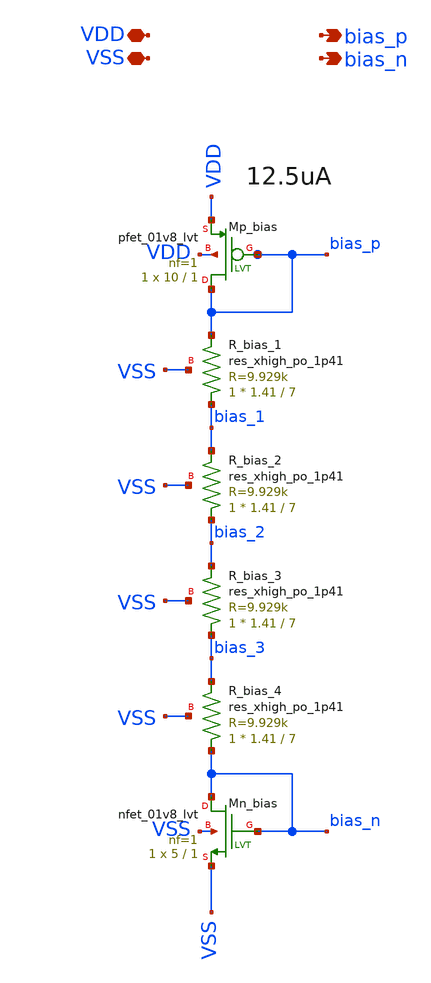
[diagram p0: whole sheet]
** sch_path: xsch/ip/vbias_generation/vbias_generation.sch
**.subckt vbias_generation bias_p VDD VSS bias_n
*.opin bias_p
*.iopin VDD
*.iopin VSS
*.opin bias_n
XR_bias_1 bias_1 bias_p VSS sky130_fd_pr__res_xhigh_po_1p41 L=7 mult=1 m=1
XMn_bias bias_n bias_n VSS VSS sky130_fd_pr__nfet_01v8_lvt L=1 W=5 nf=1 ad='int((nf+1)/2) * W/nf * 0.29'
+ as='int((nf+2)/2) * W/nf * 0.29' pd='2*int((nf+1)/2) * (W/nf + 0.29)' ps='2*int((nf+2)/2) * (W/nf + 0.29)'
+ nrd='0.29 / W' nrs='0.29 / W' sa=0 sb=0 sd=0 mult=1 m=1
XMp_bias bias_p bias_p VDD VDD sky130_fd_pr__pfet_01v8_lvt L=1 W=10 nf=1 ad='int((nf+1)/2) * W/nf * 0.29'
+ as='int((nf+2)/2) * W/nf * 0.29' pd='2*int((nf+1)/2) * (W/nf + 0.29)' ps='2*int((nf+2)/2) * (W/nf + 0.29)'
+ nrd='0.29 / W' nrs='0.29 / W' sa=0 sb=0 sd=0 mult=1 m=1
XR_bias_2 bias_2 bias_1 VSS sky130_fd_pr__res_xhigh_po_1p41 L=7 mult=1 m=1
XR_bias_3 bias_3 bias_2 VSS sky130_fd_pr__res_xhigh_po_1p41 L=7 mult=1 m=1
XR_bias_4 bias_n bias_3 VSS sky130_fd_pr__res_xhigh_po_1p41 L=7 mult=1 m=1
**.ends
.end
